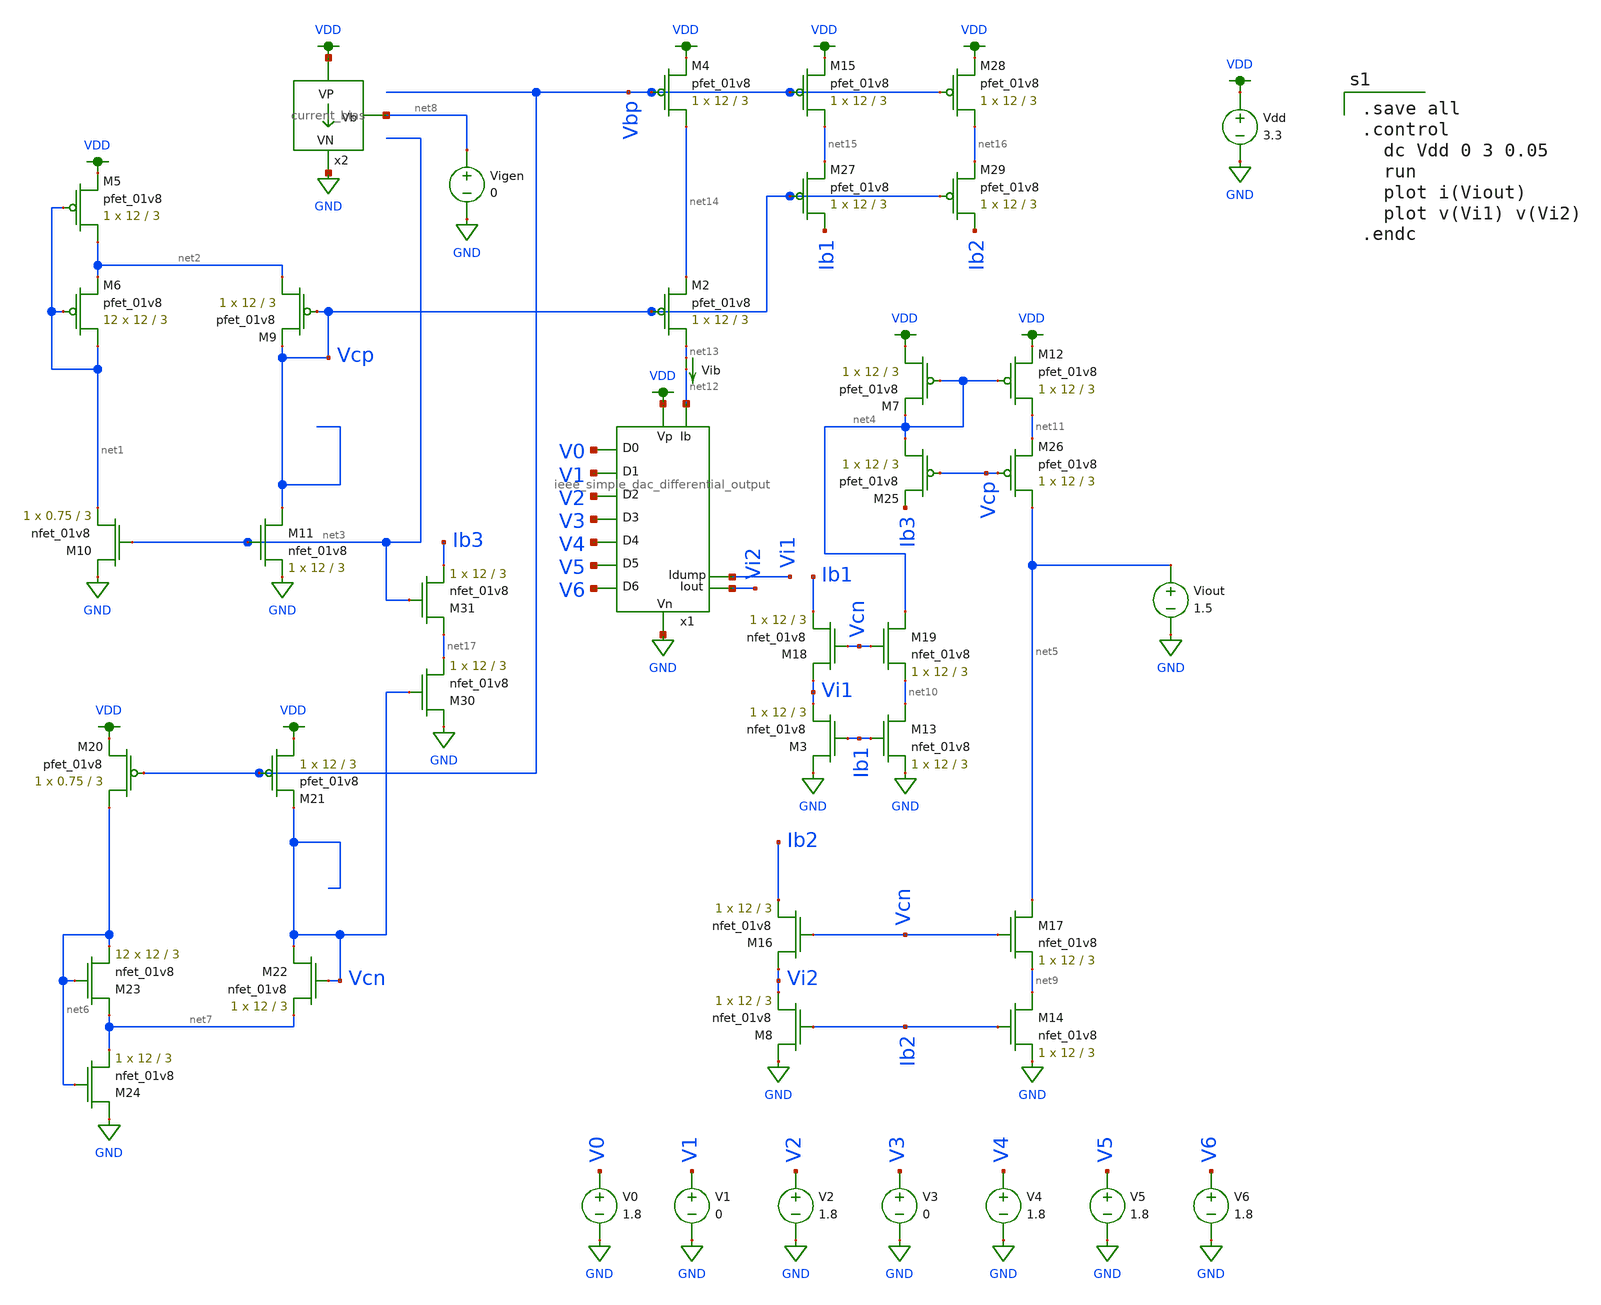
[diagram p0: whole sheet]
** sch_path: schematics/ieee DAC/ieee_DAC_mc_simulation_9.sch
**.subckt ieee_DAC_mc_simulation_9
Vdd VDD GND 3.3
V1 V1 GND 0
V2 V2 GND 1.8
V3 V3 GND 0
V4 V4 GND 1.8
V5 V5 GND 1.8
V6 V6 GND 1.8
V0 V0 GND 1.8
XM5 net2 net1 VDD VDD sky130_fd_pr__pfet_01v8 L=3 W=12 nf=1 ad='int((nf+1)/2) * W/nf * 0.29' as='int((nf+2)/2) * W/nf * 0.29'
+ pd='2*int((nf+1)/2) * (W/nf + 0.29)' ps='2*int((nf+2)/2) * (W/nf + 0.29)' nrd='0.29 / W' nrs='0.29 / W'
+ sa=0 sb=0 sd=0 mult=1 m=1
XM6 net1 net1 net2 VDD sky130_fd_pr__pfet_01v8 L=3 W=12 nf=1 ad='int((nf+1)/2) * W/nf * 0.29' as='int((nf+2)/2) * W/nf * 0.29'
+ pd='2*int((nf+1)/2) * (W/nf + 0.29)' ps='2*int((nf+2)/2) * (W/nf + 0.29)' nrd='0.29 / W' nrs='0.29 / W'
+ sa=0 sb=0 sd=0 mult=12 m=12
XM9 net2 Vcp Vcp VDD sky130_fd_pr__pfet_01v8 L=3 W=12 nf=1 ad='int((nf+1)/2) * W/nf * 0.29' as='int((nf+2)/2) * W/nf * 0.29'
+ pd='2*int((nf+1)/2) * (W/nf + 0.29)' ps='2*int((nf+2)/2) * (W/nf + 0.29)' nrd='0.29 / W' nrs='0.29 / W'
+ sa=0 sb=0 sd=0 mult=1 m=1
XM10 GND net3 net1 GND sky130_fd_pr__nfet_01v8 L=3 W=0.75 nf=1 ad='int((nf+1)/2) * W/nf * 0.29' as='int((nf+2)/2) * W/nf * 0.29'
+ pd='2*int((nf+1)/2) * (W/nf + 0.29)' ps='2*int((nf+2)/2) * (W/nf + 0.29)' nrd='0.29 / W' nrs='0.29 / W'
+ sa=0 sb=0 sd=0 mult=1 m=1
XM11 Vcp net3 GND GND sky130_fd_pr__nfet_01v8 L=3 W=12 nf=1 ad='int((nf+1)/2) * W/nf * 0.29' as='int((nf+2)/2) * W/nf * 0.29'
+ pd='2*int((nf+1)/2) * (W/nf + 0.29)' ps='2*int((nf+2)/2) * (W/nf + 0.29)' nrd='0.29 / W' nrs='0.29 / W'
+ sa=0 sb=0 sd=0 mult=1 m=1
x2 VDD net8 GND current_bias
Vigen net8 GND 0
XM3 GND Ib1 Vi1 GND sky130_fd_pr__nfet_01v8 L=3 W=12 nf=1 ad='int((nf+1)/2) * W/nf * 0.29' as='int((nf+2)/2) * W/nf * 0.29'
+ pd='2*int((nf+1)/2) * (W/nf + 0.29)' ps='2*int((nf+2)/2) * (W/nf + 0.29)' nrd='0.29 / W' nrs='0.29 / W'
+ sa=0 sb=0 sd=0 mult=1 m=1
XM7 VDD net4 net4 VDD sky130_fd_pr__pfet_01v8 L=3 W=12 nf=1 ad='int((nf+1)/2) * W/nf * 0.29' as='int((nf+2)/2) * W/nf * 0.29'
+ pd='2*int((nf+1)/2) * (W/nf + 0.29)' ps='2*int((nf+2)/2) * (W/nf + 0.29)' nrd='0.29 / W' nrs='0.29 / W'
+ sa=0 sb=0 sd=0 mult=1 m=1
XM8 GND Ib2 Vi2 GND sky130_fd_pr__nfet_01v8 L=3 W=12 nf=1 ad='int((nf+1)/2) * W/nf * 0.29' as='int((nf+2)/2) * W/nf * 0.29'
+ pd='2*int((nf+1)/2) * (W/nf + 0.29)' ps='2*int((nf+2)/2) * (W/nf + 0.29)' nrd='0.29 / W' nrs='0.29 / W'
+ sa=0 sb=0 sd=0 mult=1 m=1
XM12 net11 net4 VDD VDD sky130_fd_pr__pfet_01v8 L=3 W=12 nf=1 ad='int((nf+1)/2) * W/nf * 0.29' as='int((nf+2)/2) * W/nf * 0.29'
+ pd='2*int((nf+1)/2) * (W/nf + 0.29)' ps='2*int((nf+2)/2) * (W/nf + 0.29)' nrd='0.29 / W' nrs='0.29 / W'
+ sa=0 sb=0 sd=0 mult=1 m=1
Viout net5 GND 1.5
XM13 net10 Ib1 GND GND sky130_fd_pr__nfet_01v8 L=3 W=12 nf=1 ad='int((nf+1)/2) * W/nf * 0.29' as='int((nf+2)/2) * W/nf * 0.29'
+ pd='2*int((nf+1)/2) * (W/nf + 0.29)' ps='2*int((nf+2)/2) * (W/nf + 0.29)' nrd='0.29 / W' nrs='0.29 / W'
+ sa=0 sb=0 sd=0 mult=1 m=1
XM14 net9 Ib2 GND GND sky130_fd_pr__nfet_01v8 L=3 W=12 nf=1 ad='int((nf+1)/2) * W/nf * 0.29' as='int((nf+2)/2) * W/nf * 0.29'
+ pd='2*int((nf+1)/2) * (W/nf + 0.29)' ps='2*int((nf+2)/2) * (W/nf + 0.29)' nrd='0.29 / W' nrs='0.29 / W'
+ sa=0 sb=0 sd=0 mult=1 m=1
XM20 net6 Vbp VDD VDD sky130_fd_pr__pfet_01v8 L=3 W=0.75 nf=1 ad='int((nf+1)/2) * W/nf * 0.29' as='int((nf+2)/2) * W/nf * 0.29'
+ pd='2*int((nf+1)/2) * (W/nf + 0.29)' ps='2*int((nf+2)/2) * (W/nf + 0.29)' nrd='0.29 / W' nrs='0.29 / W'
+ sa=0 sb=0 sd=0 mult=1 m=1
XM21 VDD Vbp Vcn VDD sky130_fd_pr__pfet_01v8 L=3 W=12 nf=1 ad='int((nf+1)/2) * W/nf * 0.29' as='int((nf+2)/2) * W/nf * 0.29'
+ pd='2*int((nf+1)/2) * (W/nf + 0.29)' ps='2*int((nf+2)/2) * (W/nf + 0.29)' nrd='0.29 / W' nrs='0.29 / W'
+ sa=0 sb=0 sd=0 mult=1 m=1
XM22 Vcn Vcn net7 GND sky130_fd_pr__nfet_01v8 L=3 W=12 nf=1 ad='int((nf+1)/2) * W/nf * 0.29' as='int((nf+2)/2) * W/nf * 0.29'
+ pd='2*int((nf+1)/2) * (W/nf + 0.29)' ps='2*int((nf+2)/2) * (W/nf + 0.29)' nrd='0.29 / W' nrs='0.29 / W'
+ sa=0 sb=0 sd=0 mult=1 m=1
XM23 net7 net6 net6 GND sky130_fd_pr__nfet_01v8 L=3 W=12 nf=1 ad='int((nf+1)/2) * W/nf * 0.29' as='int((nf+2)/2) * W/nf * 0.29'
+ pd='2*int((nf+1)/2) * (W/nf + 0.29)' ps='2*int((nf+2)/2) * (W/nf + 0.29)' nrd='0.29 / W' nrs='0.29 / W'
+ sa=0 sb=0 sd=0 mult=12 m=12
XM24 GND net6 net7 GND sky130_fd_pr__nfet_01v8 L=3 W=12 nf=1 ad='int((nf+1)/2) * W/nf * 0.29' as='int((nf+2)/2) * W/nf * 0.29'
+ pd='2*int((nf+1)/2) * (W/nf + 0.29)' ps='2*int((nf+2)/2) * (W/nf + 0.29)' nrd='0.29 / W' nrs='0.29 / W'
+ sa=0 sb=0 sd=0 mult=1 m=1
XM16 Vi2 Vcn Ib2 GND sky130_fd_pr__nfet_01v8 L=3 W=12 nf=1 ad='int((nf+1)/2) * W/nf * 0.29' as='int((nf+2)/2) * W/nf * 0.29'
+ pd='2*int((nf+1)/2) * (W/nf + 0.29)' ps='2*int((nf+2)/2) * (W/nf + 0.29)' nrd='0.29 / W' nrs='0.29 / W'
+ sa=0 sb=0 sd=0 mult=1 m=1
XM17 net5 Vcn net9 GND sky130_fd_pr__nfet_01v8 L=3 W=12 nf=1 ad='int((nf+1)/2) * W/nf * 0.29' as='int((nf+2)/2) * W/nf * 0.29'
+ pd='2*int((nf+1)/2) * (W/nf + 0.29)' ps='2*int((nf+2)/2) * (W/nf + 0.29)' nrd='0.29 / W' nrs='0.29 / W'
+ sa=0 sb=0 sd=0 mult=1 m=1
XM18 Vi1 Vcn Ib1 GND sky130_fd_pr__nfet_01v8 L=3 W=12 nf=1 ad='int((nf+1)/2) * W/nf * 0.29' as='int((nf+2)/2) * W/nf * 0.29'
+ pd='2*int((nf+1)/2) * (W/nf + 0.29)' ps='2*int((nf+2)/2) * (W/nf + 0.29)' nrd='0.29 / W' nrs='0.29 / W'
+ sa=0 sb=0 sd=0 mult=1 m=1
XM19 net4 Vcn net10 GND sky130_fd_pr__nfet_01v8 L=3 W=12 nf=1 ad='int((nf+1)/2) * W/nf * 0.29' as='int((nf+2)/2) * W/nf * 0.29'
+ pd='2*int((nf+1)/2) * (W/nf + 0.29)' ps='2*int((nf+2)/2) * (W/nf + 0.29)' nrd='0.29 / W' nrs='0.29 / W'
+ sa=0 sb=0 sd=0 mult=1 m=1
XM25 net4 Vcp Ib3 VDD sky130_fd_pr__pfet_01v8 L=3 W=12 nf=1 ad='int((nf+1)/2) * W/nf * 0.29' as='int((nf+2)/2) * W/nf * 0.29'
+ pd='2*int((nf+1)/2) * (W/nf + 0.29)' ps='2*int((nf+2)/2) * (W/nf + 0.29)' nrd='0.29 / W' nrs='0.29 / W'
+ sa=0 sb=0 sd=0 mult=1 m=1
XM26 net5 Vcp net11 VDD sky130_fd_pr__pfet_01v8 L=3 W=12 nf=1 ad='int((nf+1)/2) * W/nf * 0.29' as='int((nf+2)/2) * W/nf * 0.29'
+ pd='2*int((nf+1)/2) * (W/nf + 0.29)' ps='2*int((nf+2)/2) * (W/nf + 0.29)' nrd='0.29 / W' nrs='0.29 / W'
+ sa=0 sb=0 sd=0 mult=1 m=1
x1 VDD Vi1 GND V1 V0 V2 V3 V4 V5 V6 net12 Vi2 ieee_simple_dac_differential_output
Vib net13 net12 0
.save i(vib)
XM2 net13 Vcp net14 VDD sky130_fd_pr__pfet_01v8 L=3 W=12 nf=1 ad='int((nf+1)/2) * W/nf * 0.29' as='int((nf+2)/2) * W/nf * 0.29'
+ pd='2*int((nf+1)/2) * (W/nf + 0.29)' ps='2*int((nf+2)/2) * (W/nf + 0.29)' nrd='0.29 / W' nrs='0.29 / W'
+ sa=0 sb=0 sd=0 mult=1 m=1
XM4 net14 Vbp VDD VDD sky130_fd_pr__pfet_01v8 L=3 W=12 nf=1 ad='int((nf+1)/2) * W/nf * 0.29' as='int((nf+2)/2) * W/nf * 0.29'
+ pd='2*int((nf+1)/2) * (W/nf + 0.29)' ps='2*int((nf+2)/2) * (W/nf + 0.29)' nrd='0.29 / W' nrs='0.29 / W'
+ sa=0 sb=0 sd=0 mult=1 m=1
XM15 net15 Vbp VDD VDD sky130_fd_pr__pfet_01v8 L=3 W=12 nf=1 ad='int((nf+1)/2) * W/nf * 0.29' as='int((nf+2)/2) * W/nf * 0.29'
+ pd='2*int((nf+1)/2) * (W/nf + 0.29)' ps='2*int((nf+2)/2) * (W/nf + 0.29)' nrd='0.29 / W' nrs='0.29 / W'
+ sa=0 sb=0 sd=0 mult=1 m=1
XM27 Ib1 Vcp net15 VDD sky130_fd_pr__pfet_01v8 L=3 W=12 nf=1 ad='int((nf+1)/2) * W/nf * 0.29' as='int((nf+2)/2) * W/nf * 0.29'
+ pd='2*int((nf+1)/2) * (W/nf + 0.29)' ps='2*int((nf+2)/2) * (W/nf + 0.29)' nrd='0.29 / W' nrs='0.29 / W'
+ sa=0 sb=0 sd=0 mult=1 m=1
XM28 net16 Vbp VDD VDD sky130_fd_pr__pfet_01v8 L=3 W=12 nf=1 ad='int((nf+1)/2) * W/nf * 0.29' as='int((nf+2)/2) * W/nf * 0.29'
+ pd='2*int((nf+1)/2) * (W/nf + 0.29)' ps='2*int((nf+2)/2) * (W/nf + 0.29)' nrd='0.29 / W' nrs='0.29 / W'
+ sa=0 sb=0 sd=0 mult=1 m=1
XM29 Ib2 Vcp net16 VDD sky130_fd_pr__pfet_01v8 L=3 W=12 nf=1 ad='int((nf+1)/2) * W/nf * 0.29' as='int((nf+2)/2) * W/nf * 0.29'
+ pd='2*int((nf+1)/2) * (W/nf + 0.29)' ps='2*int((nf+2)/2) * (W/nf + 0.29)' nrd='0.29 / W' nrs='0.29 / W'
+ sa=0 sb=0 sd=0 mult=1 m=1
XM30 GND Vcn net17 GND sky130_fd_pr__nfet_01v8 L=3 W=12 nf=1 ad='int((nf+1)/2) * W/nf * 0.29' as='int((nf+2)/2) * W/nf * 0.29'
+ pd='2*int((nf+1)/2) * (W/nf + 0.29)' ps='2*int((nf+2)/2) * (W/nf + 0.29)' nrd='0.29 / W' nrs='0.29 / W'
+ sa=0 sb=0 sd=0 mult=1 m=1
XM31 net17 net3 Ib3 GND sky130_fd_pr__nfet_01v8 L=3 W=12 nf=1 ad='int((nf+1)/2) * W/nf * 0.29' as='int((nf+2)/2) * W/nf * 0.29'
+ pd='2*int((nf+1)/2) * (W/nf + 0.29)' ps='2*int((nf+2)/2) * (W/nf + 0.29)' nrd='0.29 / W' nrs='0.29 / W'
+ sa=0 sb=0 sd=0 mult=1 m=1
**** begin user architecture code

.option wnflag=1
.param MC_SWITCH=1.0
.lib ~/skywater/skywater-pdk/libraries/sky130_fd_pr_ngspice/latest/models/sky130.lib.spice tt


.save all
.control
  dc Vdd 0 3 0.05
  run
  plot i(Viout)
  plot v(Vi1) v(Vi2)
.endc

**** end user architecture code
**.ends
.GLOBAL GND
.GLOBAL VDD
.end
